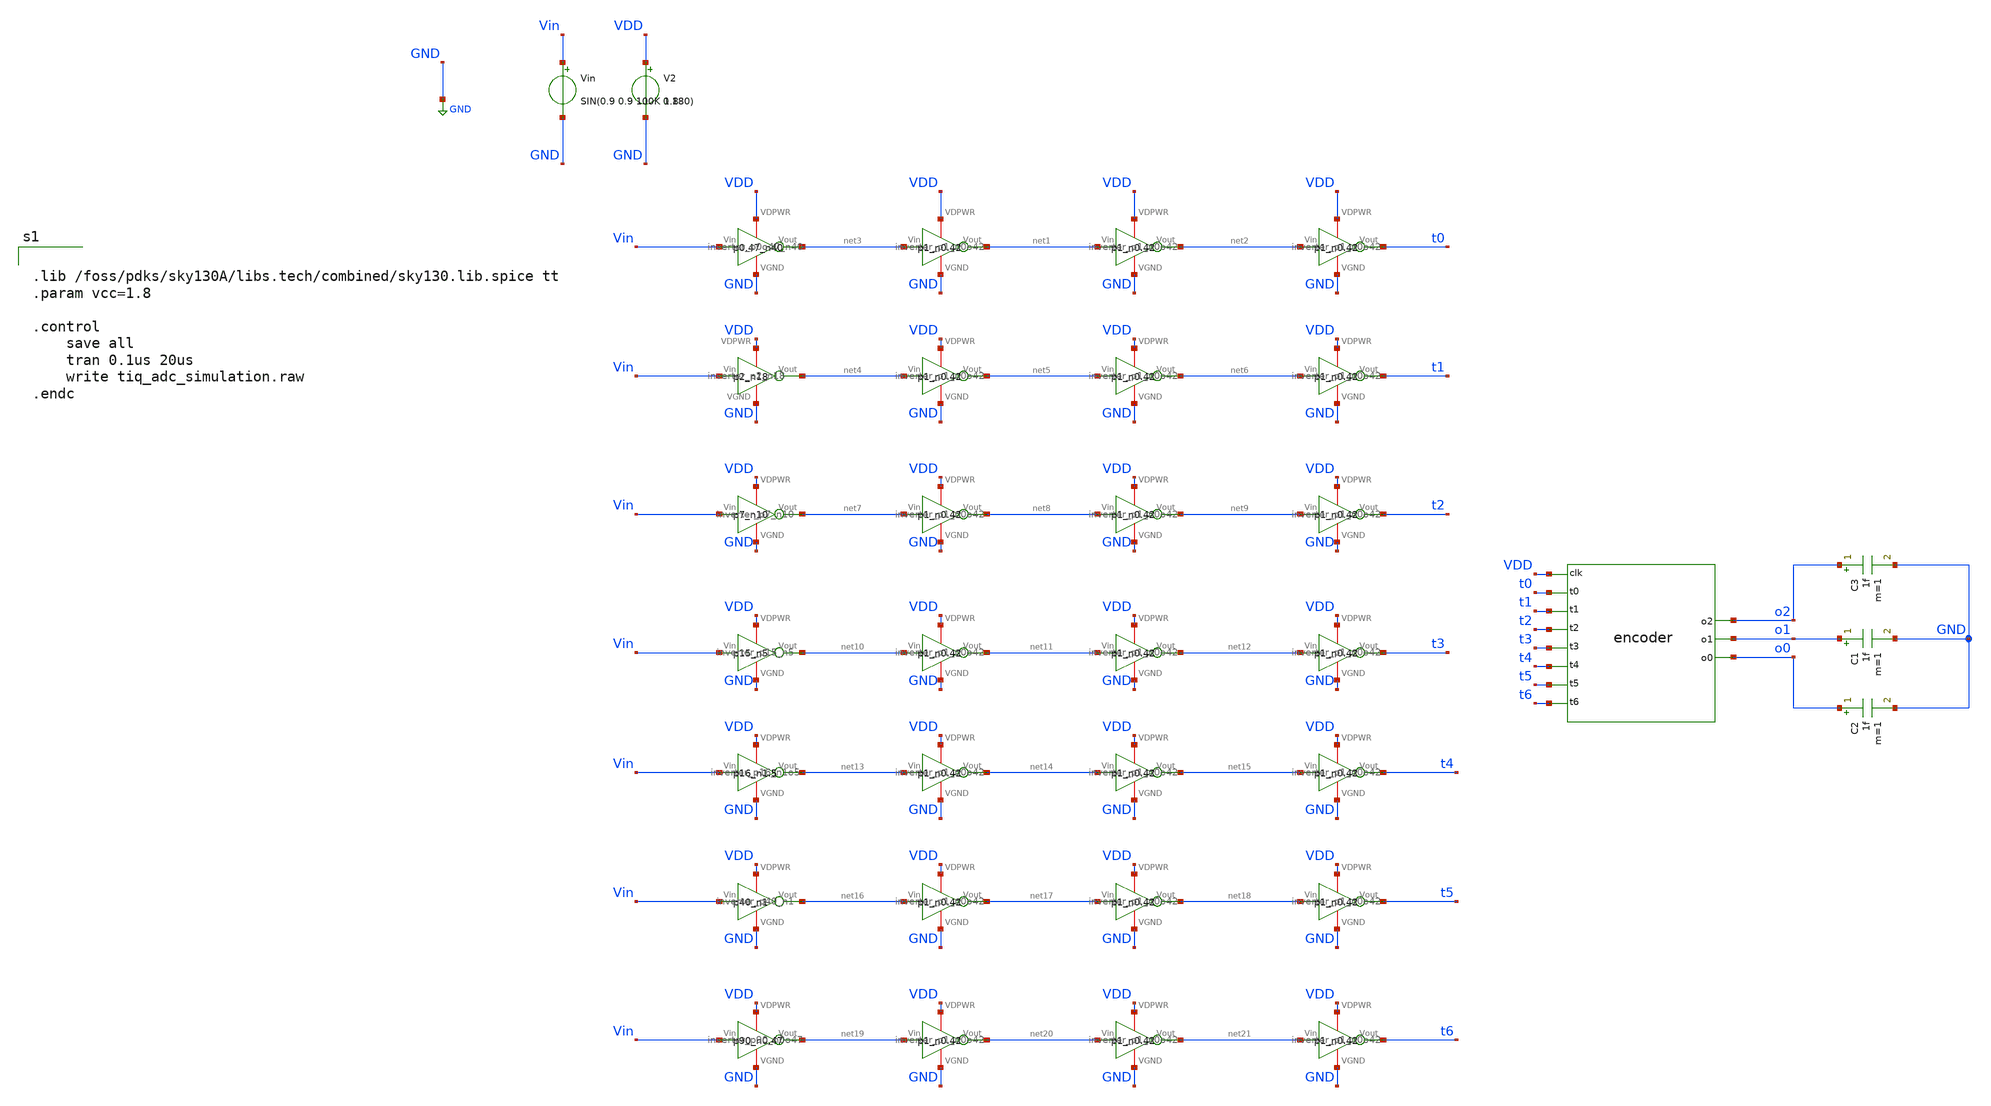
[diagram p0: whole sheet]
** sch_path: tt_um_emmersonv_tiq_adc/xschem/tiq_adc_simulation.sch
**.subckt tiq_adc_simulation
Vin Vin GND SIN(0.9 0.9 100K 0 180)
V2 VDD GND 1.8
x4 VDD net10 Vin GND inverter_p15_n5
x5 VDD net13 Vin GND inverter_p16_n1o5
x6 VDD net16 Vin GND inverter_p40_n1
x2 VDD net4 Vin GND inverter_p2_n18
x3 VDD net7 Vin GND inverter_p7_n10
x7 VDD net19 Vin GND inverter_p90_n0o47
x1 VDD net3 Vin GND inverter_p0o47_n40
C3 o2 GND 1f m=1
C1 o1 GND 1f m=1
C2 o0 GND 1f m=1
ADUT [ VDD t0 t1 t2 t3 t4 t5 t6 ] [ o0 o1 o2 ] dut
x8 VDD net1 net3 GND inverter_p1_n0o42
x9 VDD net2 net1 GND inverter_p1_n0o42
x10 VDD t0 net2 GND inverter_p1_n0o42
x11 VDD net5 net4 GND inverter_p1_n0o42
x12 VDD net6 net5 GND inverter_p1_n0o42
x13 VDD t1 net6 GND inverter_p1_n0o42
x14 VDD net8 net7 GND inverter_p1_n0o42
x15 VDD net9 net8 GND inverter_p1_n0o42
x16 VDD t2 net9 GND inverter_p1_n0o42
x17 VDD net11 net10 GND inverter_p1_n0o42
x18 VDD net12 net11 GND inverter_p1_n0o42
x19 VDD t3 net12 GND inverter_p1_n0o42
x20 VDD net14 net13 GND inverter_p1_n0o42
x21 VDD net15 net14 GND inverter_p1_n0o42
x22 VDD t4 net15 GND inverter_p1_n0o42
x23 VDD net17 net16 GND inverter_p1_n0o42
x24 VDD net18 net17 GND inverter_p1_n0o42
x25 VDD t5 net18 GND inverter_p1_n0o42
x26 VDD net20 net19 GND inverter_p1_n0o42
x27 VDD net21 net20 GND inverter_p1_n0o42
x28 VDD t6 net21 GND inverter_p1_n0o42
**** begin user architecture code


.lib /foss/pdks/sky130A/libs.tech/combined/sky130.lib.spice tt
.param vcc=1.8

.control
	save all
	tran 0.1us 20us
	write tiq_adc_simulation.raw
.endc


**** end user architecture code
**.ends

* expanding   symbol:
*+  /foss/designs/analog-circuit-design/sky25a-TIQ_ADC/xschem/INVERTER_SIZES/inverter_p15_n5.sym # of pins=4
** sym_path: tt_um_emmersonv_tiq_adc/xschem/INVERTER_SIZES/inverter_p15_n5.sym
** sch_path: tt_um_emmersonv_tiq_adc/xschem/INVERTER_SIZES/inverter_p15_n5.sch
.subckt inverter_p15_n5 VDPWR Vout Vin VGND
*.opin Vout
*.ipin Vin
*.iopin VDPWR
*.iopin VGND
XM1 Vout Vin VGND VGND sky130_fd_pr__nfet_01v8 L=0.15 W=5 nf=2 ad='int((nf+1)/2) * W/nf * 0.29' as='int((nf+2)/2) * W/nf * 0.29'
+ pd='2*int((nf+1)/2) * (W/nf + 0.29)' ps='2*int((nf+2)/2) * (W/nf + 0.29)' nrd='0.29 / W' nrs='0.29 / W'
+ sa=0 sb=0 sd=0 mult=1 m=1
XM2 Vout Vin VDPWR VDPWR sky130_fd_pr__pfet_01v8 L=0.15 W=15 nf=2 ad='int((nf+1)/2) * W/nf * 0.29' as='int((nf+2)/2) * W/nf * 0.29'
+ pd='2*int((nf+1)/2) * (W/nf + 0.29)' ps='2*int((nf+2)/2) * (W/nf + 0.29)' nrd='0.29 / W' nrs='0.29 / W'
+ sa=0 sb=0 sd=0 mult=1 m=1
.ends


* expanding   symbol:
*+  /foss/designs/analog-circuit-design/sky25a-TIQ_ADC/xschem/INVERTER_SIZES/inverter_p16_n1o5.sym # of pins=4
** sym_path: tt_um_emmersonv_tiq_adc/xschem/INVERTER_SIZES/inverter_p16_n1o5.sym
** sch_path: tt_um_emmersonv_tiq_adc/xschem/INVERTER_SIZES/inverter_p16_n1o5.sch
.subckt inverter_p16_n1o5 VDPWR Vout Vin VGND
*.opin Vout
*.ipin Vin
*.iopin VDPWR
*.iopin VGND
XM1 Vout Vin VGND VGND sky130_fd_pr__nfet_01v8 L=0.15 W=1.5 nf=1 ad='int((nf+1)/2) * W/nf * 0.29' as='int((nf+2)/2) * W/nf * 0.29'
+ pd='2*int((nf+1)/2) * (W/nf + 0.29)' ps='2*int((nf+2)/2) * (W/nf + 0.29)' nrd='0.29 / W' nrs='0.29 / W'
+ sa=0 sb=0 sd=0 mult=1 m=1
XM2 Vout Vin VDPWR VDPWR sky130_fd_pr__pfet_01v8 L=0.15 W=16 nf=2 ad='int((nf+1)/2) * W/nf * 0.29' as='int((nf+2)/2) * W/nf * 0.29'
+ pd='2*int((nf+1)/2) * (W/nf + 0.29)' ps='2*int((nf+2)/2) * (W/nf + 0.29)' nrd='0.29 / W' nrs='0.29 / W'
+ sa=0 sb=0 sd=0 mult=1 m=1
.ends


* expanding   symbol:
*+  /foss/designs/analog-circuit-design/sky25a-TIQ_ADC/xschem/INVERTER_SIZES/inverter_p40_n1.sym # of pins=4
** sym_path: tt_um_emmersonv_tiq_adc/xschem/INVERTER_SIZES/inverter_p40_n1.sym
** sch_path: tt_um_emmersonv_tiq_adc/xschem/INVERTER_SIZES/inverter_p40_n1.sch
.subckt inverter_p40_n1 VDPWR Vout Vin VGND
*.opin Vout
*.ipin Vin
*.iopin VDPWR
*.iopin VGND
XM1 Vout Vin VGND VGND sky130_fd_pr__nfet_01v8 L=0.15 W=1 nf=1 ad='int((nf+1)/2) * W/nf * 0.29' as='int((nf+2)/2) * W/nf * 0.29'
+ pd='2*int((nf+1)/2) * (W/nf + 0.29)' ps='2*int((nf+2)/2) * (W/nf + 0.29)' nrd='0.29 / W' nrs='0.29 / W'
+ sa=0 sb=0 sd=0 mult=1 m=1
XM2 Vout Vin VDPWR VDPWR sky130_fd_pr__pfet_01v8 L=0.15 W=20 nf=2 ad='int((nf+1)/2) * W/nf * 0.29' as='int((nf+2)/2) * W/nf * 0.29'
+ pd='2*int((nf+1)/2) * (W/nf + 0.29)' ps='2*int((nf+2)/2) * (W/nf + 0.29)' nrd='0.29 / W' nrs='0.29 / W'
+ sa=0 sb=0 sd=0 mult=1 m=1
XM3 Vout Vin VDPWR VDPWR sky130_fd_pr__pfet_01v8 L=0.15 W=20 nf=2 ad='int((nf+1)/2) * W/nf * 0.29' as='int((nf+2)/2) * W/nf * 0.29'
+ pd='2*int((nf+1)/2) * (W/nf + 0.29)' ps='2*int((nf+2)/2) * (W/nf + 0.29)' nrd='0.29 / W' nrs='0.29 / W'
+ sa=0 sb=0 sd=0 mult=1 m=1
.ends


* expanding   symbol:
*+  /foss/designs/analog-circuit-design/sky25a-TIQ_ADC/xschem/INVERTER_SIZES/inverter_p2_n18.sym # of pins=4
** sym_path: tt_um_emmersonv_tiq_adc/xschem/INVERTER_SIZES/inverter_p2_n18.sym
** sch_path: tt_um_emmersonv_tiq_adc/xschem/INVERTER_SIZES/inverter_p2_n18.sch
.subckt inverter_p2_n18 VDPWR Vout Vin VGND
*.opin Vout
*.ipin Vin
*.iopin VDPWR
*.iopin VGND
XM1 Vout Vin VGND VGND sky130_fd_pr__nfet_01v8 L=0.15 W=9 nf=2 ad='int((nf+1)/2) * W/nf * 0.29' as='int((nf+2)/2) * W/nf * 0.29'
+ pd='2*int((nf+1)/2) * (W/nf + 0.29)' ps='2*int((nf+2)/2) * (W/nf + 0.29)' nrd='0.29 / W' nrs='0.29 / W'
+ sa=0 sb=0 sd=0 mult=1 m=1
XM2 Vout Vin VDPWR VDPWR sky130_fd_pr__pfet_01v8 L=0.15 W=2 nf=1 ad='int((nf+1)/2) * W/nf * 0.29' as='int((nf+2)/2) * W/nf * 0.29'
+ pd='2*int((nf+1)/2) * (W/nf + 0.29)' ps='2*int((nf+2)/2) * (W/nf + 0.29)' nrd='0.29 / W' nrs='0.29 / W'
+ sa=0 sb=0 sd=0 mult=1 m=1
XM3 Vout Vin VGND VGND sky130_fd_pr__nfet_01v8 L=0.15 W=9 nf=2 ad='int((nf+1)/2) * W/nf * 0.29' as='int((nf+2)/2) * W/nf * 0.29'
+ pd='2*int((nf+1)/2) * (W/nf + 0.29)' ps='2*int((nf+2)/2) * (W/nf + 0.29)' nrd='0.29 / W' nrs='0.29 / W'
+ sa=0 sb=0 sd=0 mult=1 m=1
.ends


* expanding   symbol:
*+  /foss/designs/analog-circuit-design/sky25a-TIQ_ADC/xschem/INVERTER_SIZES/inverter_p7_n10.sym # of pins=4
** sym_path: tt_um_emmersonv_tiq_adc/xschem/INVERTER_SIZES/inverter_p7_n10.sym
** sch_path: tt_um_emmersonv_tiq_adc/xschem/INVERTER_SIZES/inverter_p7_n10.sch
.subckt inverter_p7_n10 VDPWR Vout Vin VGND
*.opin Vout
*.ipin Vin
*.iopin VDPWR
*.iopin VGND
XM1 Vout Vin VGND VGND sky130_fd_pr__nfet_01v8 L=0.15 W=5 nf=2 ad='int((nf+1)/2) * W/nf * 0.29' as='int((nf+2)/2) * W/nf * 0.29'
+ pd='2*int((nf+1)/2) * (W/nf + 0.29)' ps='2*int((nf+2)/2) * (W/nf + 0.29)' nrd='0.29 / W' nrs='0.29 / W'
+ sa=0 sb=0 sd=0 mult=1 m=1
XM2 Vout Vin VDPWR VDPWR sky130_fd_pr__pfet_01v8 L=0.15 W=7 nf=1 ad='int((nf+1)/2) * W/nf * 0.29' as='int((nf+2)/2) * W/nf * 0.29'
+ pd='2*int((nf+1)/2) * (W/nf + 0.29)' ps='2*int((nf+2)/2) * (W/nf + 0.29)' nrd='0.29 / W' nrs='0.29 / W'
+ sa=0 sb=0 sd=0 mult=1 m=1
XM3 Vout Vin VGND VGND sky130_fd_pr__nfet_01v8 L=0.15 W=5 nf=2 ad='int((nf+1)/2) * W/nf * 0.29' as='int((nf+2)/2) * W/nf * 0.29'
+ pd='2*int((nf+1)/2) * (W/nf + 0.29)' ps='2*int((nf+2)/2) * (W/nf + 0.29)' nrd='0.29 / W' nrs='0.29 / W'
+ sa=0 sb=0 sd=0 mult=1 m=1
.ends


* expanding   symbol:
*+  /foss/designs/analog-circuit-design/sky25a-TIQ_ADC/xschem/INVERTER_SIZES/inverter_p90_n0o47.sym # of pins=4
** sym_path: tt_um_emmersonv_tiq_adc/xschem/INVERTER_SIZES/inverter_p90_n0o47.sym
** sch_path: tt_um_emmersonv_tiq_adc/xschem/INVERTER_SIZES/inverter_p90_n0o47.sch
.subckt inverter_p90_n0o47 VDPWR Vout Vin VGND
*.opin Vout
*.ipin Vin
*.iopin VDPWR
*.iopin VGND
XM1 Vout Vin VGND VGND sky130_fd_pr__nfet_01v8 L=0.15 W=0.47 nf=1 ad='int((nf+1)/2) * W/nf * 0.29' as='int((nf+2)/2) * W/nf * 0.29'
+ pd='2*int((nf+1)/2) * (W/nf + 0.29)' ps='2*int((nf+2)/2) * (W/nf + 0.29)' nrd='0.29 / W' nrs='0.29 / W'
+ sa=0 sb=0 sd=0 mult=1 m=1
XM2 Vout Vin VDPWR VDPWR sky130_fd_pr__pfet_01v8 L=0.15 W=30 nf=3 ad='int((nf+1)/2) * W/nf * 0.29' as='int((nf+2)/2) * W/nf * 0.29'
+ pd='2*int((nf+1)/2) * (W/nf + 0.29)' ps='2*int((nf+2)/2) * (W/nf + 0.29)' nrd='0.29 / W' nrs='0.29 / W'
+ sa=0 sb=0 sd=0 mult=1 m=1
XM3 Vout Vin VDPWR VDPWR sky130_fd_pr__pfet_01v8 L=0.15 W=30 nf=3 ad='int((nf+1)/2) * W/nf * 0.29' as='int((nf+2)/2) * W/nf * 0.29'
+ pd='2*int((nf+1)/2) * (W/nf + 0.29)' ps='2*int((nf+2)/2) * (W/nf + 0.29)' nrd='0.29 / W' nrs='0.29 / W'
+ sa=0 sb=0 sd=0 mult=1 m=1
XM4 Vout Vin VDPWR VDPWR sky130_fd_pr__pfet_01v8 L=0.15 W=30 nf=3 ad='int((nf+1)/2) * W/nf * 0.29' as='int((nf+2)/2) * W/nf * 0.29'
+ pd='2*int((nf+1)/2) * (W/nf + 0.29)' ps='2*int((nf+2)/2) * (W/nf + 0.29)' nrd='0.29 / W' nrs='0.29 / W'
+ sa=0 sb=0 sd=0 mult=1 m=1
.ends


* expanding   symbol:
*+  /foss/designs/analog-circuit-design/sky25a-TIQ_ADC/xschem/INVERTER_SIZES/inverter_p0o47_n40.sym # of pins=4
** sym_path: tt_um_emmersonv_tiq_adc/xschem/INVERTER_SIZES/inverter_p0o47_n40.sym
** sch_path: tt_um_emmersonv_tiq_adc/xschem/INVERTER_SIZES/inverter_p0o47_n40.sch
.subckt inverter_p0o47_n40 VDPWR Vout Vin VGND
*.opin Vout
*.ipin Vin
*.iopin VDPWR
*.iopin VGND
XM1 Vout Vin VGND VGND sky130_fd_pr__nfet_01v8 L=0.15 W=13.33 nf=2 ad='int((nf+1)/2) * W/nf * 0.29' as='int((nf+2)/2) * W/nf * 0.29'
+ pd='2*int((nf+1)/2) * (W/nf + 0.29)' ps='2*int((nf+2)/2) * (W/nf + 0.29)' nrd='0.29 / W' nrs='0.29 / W'
+ sa=0 sb=0 sd=0 mult=1 m=1
XM2 Vout Vin VDPWR VDPWR sky130_fd_pr__pfet_01v8 L=0.15 W=0.47 nf=1 ad='int((nf+1)/2) * W/nf * 0.29'
+ as='int((nf+2)/2) * W/nf * 0.29' pd='2*int((nf+1)/2) * (W/nf + 0.29)' ps='2*int((nf+2)/2) * (W/nf + 0.29)'
+ nrd='0.29 / W' nrs='0.29 / W' sa=0 sb=0 sd=0 mult=1 m=1
XM3 Vout Vin VGND VGND sky130_fd_pr__nfet_01v8 L=0.15 W=13.33 nf=2 ad='int((nf+1)/2) * W/nf * 0.29' as='int((nf+2)/2) * W/nf * 0.29'
+ pd='2*int((nf+1)/2) * (W/nf + 0.29)' ps='2*int((nf+2)/2) * (W/nf + 0.29)' nrd='0.29 / W' nrs='0.29 / W'
+ sa=0 sb=0 sd=0 mult=1 m=1
XM4 Vout Vin VGND VGND sky130_fd_pr__nfet_01v8 L=0.15 W=13.33 nf=2 ad='int((nf+1)/2) * W/nf * 0.29' as='int((nf+2)/2) * W/nf * 0.29'
+ pd='2*int((nf+1)/2) * (W/nf + 0.29)' ps='2*int((nf+2)/2) * (W/nf + 0.29)' nrd='0.29 / W' nrs='0.29 / W'
+ sa=0 sb=0 sd=0 mult=1 m=1
.ends


* expanding   symbol:
*+  /foss/designs/analog-circuit-design/sky25a-TIQ_ADC/xschem/INVERTER_SIZES/inverter_p1_n0o42.sym # of pins=4
** sym_path: tt_um_emmersonv_tiq_adc/xschem/INVERTER_SIZES/inverter_p1_n0o42.sym
** sch_path: tt_um_emmersonv_tiq_adc/xschem/INVERTER_SIZES/inverter_p1_n0o42.sch
.subckt inverter_p1_n0o42 VDPWR Vout Vin VGND
*.opin Vout
*.ipin Vin
*.iopin VDPWR
*.iopin VGND
XM1 Vout Vin VGND VGND sky130_fd_pr__nfet_01v8 L=0.15 W=0.42 nf=1 ad='int((nf+1)/2) * W/nf * 0.29' as='int((nf+2)/2) * W/nf * 0.29'
+ pd='2*int((nf+1)/2) * (W/nf + 0.29)' ps='2*int((nf+2)/2) * (W/nf + 0.29)' nrd='0.29 / W' nrs='0.29 / W'
+ sa=0 sb=0 sd=0 mult=1 m=1
XM2 Vout Vin VDPWR VDPWR sky130_fd_pr__pfet_01v8 L=0.15 W=1 nf=1 ad='int((nf+1)/2) * W/nf * 0.29' as='int((nf+2)/2) * W/nf * 0.29'
+ pd='2*int((nf+1)/2) * (W/nf + 0.29)' ps='2*int((nf+2)/2) * (W/nf + 0.29)' nrd='0.29 / W' nrs='0.29 / W'
+ sa=0 sb=0 sd=0 mult=1 m=1
.ends

.GLOBAL GND
**** begin user architecture code
.model dut d_cosim simulation="./encoder.so"
**** end user architecture code
.end
